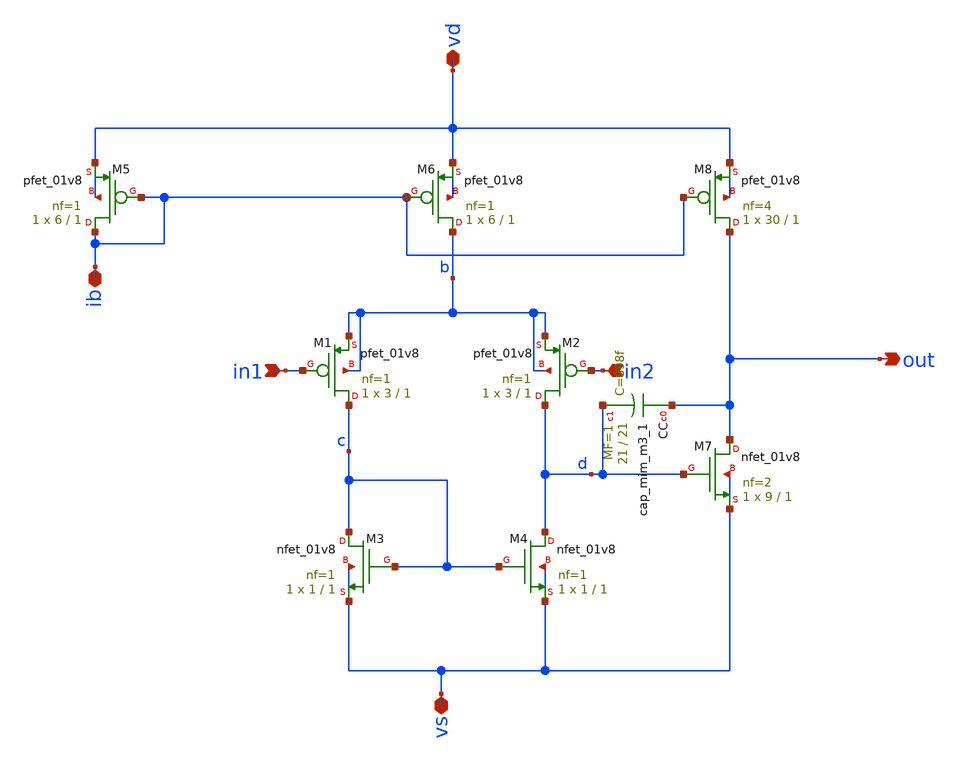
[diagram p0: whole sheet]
** sch_path: ota/xschem/ota.sch
* Copyright 2020 Stefan Frederik Schippers
* Licensed under the Apache License, Version 2.0 (the "License");
* you may not use this file except in compliance with the License.
* You may obtain a copy of the License at
* https://www.apache.org/licenses/LICENSE-2.0
* Unless required by applicable law or agreed to in writing, software
* distributed under the License is distributed on an "AS IS" BASIS,
* WITHOUT WARRANTIES OR CONDITIONS OF ANY KIND, either express or implied.
* See the License for the specific language governing permissions and
* limitations under the License.
**.subckt ota vd vs ib in1 in2 out
*.iopin vd
*.iopin vs
*.iopin ib
*.ipin in1
*.ipin in2
*.opin out
XCC out d sky130_fd_pr__cap_mim_m3_1 W=21 L=21 MF=1 m=1
XM5 ib ib vd vd sky130_fd_pr__pfet_01v8 L=1 W=6 nf=1 ad='int((nf+1)/2) * W/nf * 0.29' as='int((nf+2)/2) * W/nf * 0.29'
+ pd='2*int((nf+1)/2) * (W/nf + 0.29)' ps='2*int((nf+2)/2) * (W/nf + 0.29)' nrd='0.29 / W' nrs='0.29 / W'
+ sa=0 sb=0 sd=0 mult=1 m=1
XM6 b ib vd vd sky130_fd_pr__pfet_01v8 L=1 W=6 nf=1 ad='int((nf+1)/2) * W/nf * 0.29' as='int((nf+2)/2) * W/nf * 0.29'
+ pd='2*int((nf+1)/2) * (W/nf + 0.29)' ps='2*int((nf+2)/2) * (W/nf + 0.29)' nrd='0.29 / W' nrs='0.29 / W'
+ sa=0 sb=0 sd=0 mult=1 m=1
XM8 out ib vd vd sky130_fd_pr__pfet_01v8 L=1 W=30 nf=4 ad='int((nf+1)/2) * W/nf * 0.29' as='int((nf+2)/2) * W/nf * 0.29'
+ pd='2*int((nf+1)/2) * (W/nf + 0.29)' ps='2*int((nf+2)/2) * (W/nf + 0.29)' nrd='0.29 / W' nrs='0.29 / W'
+ sa=0 sb=0 sd=0 mult=1 m=1
XM1 c in1 b b sky130_fd_pr__pfet_01v8 L=1 W=3 nf=1 ad='int((nf+1)/2) * W/nf * 0.29' as='int((nf+2)/2) * W/nf * 0.29'
+ pd='2*int((nf+1)/2) * (W/nf + 0.29)' ps='2*int((nf+2)/2) * (W/nf + 0.29)' nrd='0.29 / W' nrs='0.29 / W'
+ sa=0 sb=0 sd=0 mult=1 m=1
XM2 d in2 b b sky130_fd_pr__pfet_01v8 L=1 W=3 nf=1 ad='int((nf+1)/2) * W/nf * 0.29' as='int((nf+2)/2) * W/nf * 0.29'
+ pd='2*int((nf+1)/2) * (W/nf + 0.29)' ps='2*int((nf+2)/2) * (W/nf + 0.29)' nrd='0.29 / W' nrs='0.29 / W'
+ sa=0 sb=0 sd=0 mult=1 m=1
XM3 c c vs vs sky130_fd_pr__nfet_01v8 L=1 W=1 nf=1 ad='int((nf+1)/2) * W/nf * 0.29' as='int((nf+2)/2) * W/nf * 0.29'
+ pd='2*int((nf+1)/2) * (W/nf + 0.29)' ps='2*int((nf+2)/2) * (W/nf + 0.29)' nrd='0.29 / W' nrs='0.29 / W'
+ sa=0 sb=0 sd=0 mult=1 m=1
XM4 d c vs vs sky130_fd_pr__nfet_01v8 L=1 W=1 nf=1 ad='int((nf+1)/2) * W/nf * 0.29' as='int((nf+2)/2) * W/nf * 0.29'
+ pd='2*int((nf+1)/2) * (W/nf + 0.29)' ps='2*int((nf+2)/2) * (W/nf + 0.29)' nrd='0.29 / W' nrs='0.29 / W'
+ sa=0 sb=0 sd=0 mult=1 m=1
XM7 out d vs vs sky130_fd_pr__nfet_01v8 L=1 W=9 nf=2 ad='int((nf+1)/2) * W/nf * 0.29' as='int((nf+2)/2) * W/nf * 0.29'
+ pd='2*int((nf+1)/2) * (W/nf + 0.29)' ps='2*int((nf+2)/2) * (W/nf + 0.29)' nrd='0.29 / W' nrs='0.29 / W'
+ sa=0 sb=0 sd=0 mult=1 m=1
**** begin user architecture code


R0 out out.t0 2.193
R1 in1 in1.t0 89
R2 in2 in2.t0 89.543
R3 vs.n0 vs.n4 362.164
R4 vs.n0 vs.n2 362.164
R5 vs.n27 vs.n22 181.834
R6 vs.n12 vs.n7 181.834
R7 vs.n16 vs.n15 108.422
R8 vs.n28 vs.n27 108.422
R9 vs.n0 vs.n5 108.422
R10 vs.n13 vs.n12 108.422
R11 vs.n30 vs.n29 0.979
R12 vs.n17 vs.n14 0.148
R13 vs.n30 vs 0.062
R14 vs.n20 vs.n17 0.061
R15 vs.n29 vs.n20 0.061
R16 vs.n14 vs.n0 0.061
R17 vs.n22 vs.n21 0.046
R18 vs.n7 vs.n6 0.046
R19 vs.n27 vs.n26 0.042
R20 vs.n12 vs.n11 0.042
R21 vs.n25 vs.n24 0.035
R22 vs.n10 vs.n9 0.035
R23 vs vs.n30 0.026
R24 vs.n24 vs.n23 0.025
R25 vs.n9 vs.n8 0.025
R26 vs.n26 vs.n25 0.025
R27 vs.n11 vs.n10 0.025
R28 vs.n14 vs.n13 0.017
R29 vs.n17 vs.n16 0.017
R30 vs.n29 vs.n28 0.017
R31 vs.n4 vs.n3 0.013
R32 vs.n2 vs.n1 0.013
R33 vs.n19 vs.n18 0.001
R34 vs.n20 vs.n19 0.001
R35 ib.n0 ib.t5 196.349
R36 ib.n2 ib.t4 196.205
R37 ib.n1 ib.t3 196.185
R38 ib.n0 ib.t6 196.183
R39 ib.t0 ib.n3 160.591
R40 ib.n4 ib.t0 160.08
R41 ib.n3 ib.t2 160.055
R42 ib.n4 ib.t1 5.789
R43 ib ib.n4 1.164
R44 ib.n3 ib.n2 1.125
R45 ib.n2 ib.n1 0.175
R46 ib.n1 ib.n0 0.162
R47 vd.n28 vd.n27 251.205
R48 vd.n21 vd.n20 248.846
R49 vd.n8 vd.n7 105.107
R50 vd.n18 vd.n17 105.107
R51 vd.n2 vd.n1 103.152
R52 vd.n12 vd.n11 103.152
R53 vd.n29 vd.n28 1.606
R54 vd.n9 vd.n8 1.199
R55 vd.n19 vd.n18 1.199
R56 vd.n30 vd.n29 0.975
R57 vd vd.n9 0.594
R58 vd vd.n30 0.576
R59 vd.n29 vd.n21 0.389
R60 vd.n19 vd.n12 0.389
R61 vd.n9 vd.n2 0.334
R62 vd.n30 vd.n19 0.054
R63 vd.n1 vd.n0 0.015
R64 vd.n11 vd.n10 0.015
R65 vd.n27 vd.n26 0.004
R66 vd.n24 vd.n23 0.003
R67 vd.n4 vd.n3 0.003
R68 vd.n14 vd.n13 0.003
R69 vd.n5 vd.n4 0.003
R70 vd.n15 vd.n14 0.003
R71 vd.n23 vd.n22 0.003
R72 vd.n25 vd.n24 0.001
R73 vd.n6 vd.n5 0.001
R74 vd.n16 vd.n15 0.001
R75 vd.n8 vd.n6 0.001
R76 vd.n28 vd.n25 0.001
R77 vd.n18 vd.n16 0.001
C0 ib m1_420_6300# 0.22fF
C1 out vd 0.58fF
C2 in2 vd 0.08fF
C3 m1_1300_5200# ib 0.23fF
C4 out in2 0.02fF
C5 in1 m1_420_6300# 0.21fF
C6 vd ib 2.47fF
C7 out ib 0.59fF
C8 in2 ib 0.08fF
C9 m1_1300_5200# in1 0.02fF
C10 m1_n20_5200# in1 0.25fF
C11 m1_1300_5200# m1_420_6300# 0.32fF
C12 m1_n20_5200# m1_420_6300# 0.51fF
C13 in1 vd 0.08fF
C14 m1_n20_5200# m1_1300_5200# 0.24fF
C15 in1 in2 0.28fF
C16 vd m1_420_6300# 0.65fF
C17 out m1_420_6300# 0.01fF
C18 in2 m1_420_6300# 0.48fF
C19 m1_1300_5200# vd 0.23fF
C20 m1_n20_5200# vd 0.01fF
C21 m1_1300_5200# out 1.30fF
C22 m1_1300_5200# in2 0.16fF
C23 m1_n20_5200# out 0.05fF
C24 in1 ib 0.24fF
C25 m1_n20_5200# in2 0.55fF
C26 vd.n0 vs 0.94fF $ **FLOATING
C27 vd.n1 vs 0.07fF $ **FLOATING
C28 vd.n2 vs 0.07fF $ **FLOATING
C29 vd.n3 vs 0.11fF $ **FLOATING
C30 vd.n4 vs 0.11fF $ **FLOATING
C31 vd.n6 vs 1.65fF $ **FLOATING
C32 vd.n7 vs 1.01fF $ **FLOATING
C33 vd.n8 vs 0.20fF $ **FLOATING
C34 vd.n9 vs 0.87fF $ **FLOATING
C35 vd.n10 vs 0.94fF $ **FLOATING
C36 vd.n11 vs 0.07fF $ **FLOATING
C37 vd.n12 vs 0.07fF $ **FLOATING
C38 vd.n13 vs 0.11fF $ **FLOATING
C39 vd.n14 vs 0.11fF $ **FLOATING
C40 vd.n16 vs 1.65fF $ **FLOATING
C41 vd.n17 vs 1.01fF $ **FLOATING
C42 vd.n18 vs 0.20fF $ **FLOATING
C43 vd.n19 vs 0.63fF $ **FLOATING
C44 vd.n20 vs 2.53fF $ **FLOATING
C45 vd.n21 vs 0.10fF $ **FLOATING
C46 vd.n22 vs 0.17fF $ **FLOATING
C47 vd.n23 vs 0.17fF $ **FLOATING
C48 vd.n25 vs 4.29fF $ **FLOATING
C49 vd.n26 vs 2.41fF $ **FLOATING
C50 vd.n27 vs 0.12fF $ **FLOATING
C51 vd.n28 vs 0.26fF $ **FLOATING
C52 vd.n29 vs 2.37fF $ **FLOATING
C53 vd.n30 vs 0.52fF $ **FLOATING
C54 ib.t1 vs 0.10fF
C55 ib.t2 vs 0.56fF
C56 ib.t4 vs 0.67fF
C57 ib.t3 vs 0.67fF
C58 ib.t6 vs 0.67fF
C59 ib.t5 vs 0.67fF
C60 ib.n0 vs 0.85fF $ **FLOATING
C61 ib.n1 vs 0.42fF $ **FLOATING
C62 ib.n2 vs 0.82fF $ **FLOATING
C63 ib.n3 vs 1.45fF $ **FLOATING
C64 ib.t0 vs 0.34fF
C65 ib.n4 vs 1.16fF $ **FLOATING
C66 out.t0 vs 43.11fF
C67 vd vs 18.09fF
C68 ib vs 3.61fF
C69 in2 vs 1.62fF
C70 m1_420_6300# vs 5.04fF
C71 m1_n20_5200# vs 2.57fF
C72 in1 vs 0.94fF
C73 out vs 7.60fF
C74 m1_1300_5200# vs 13.94fF


**** end user architecture code
**.ends
.end
